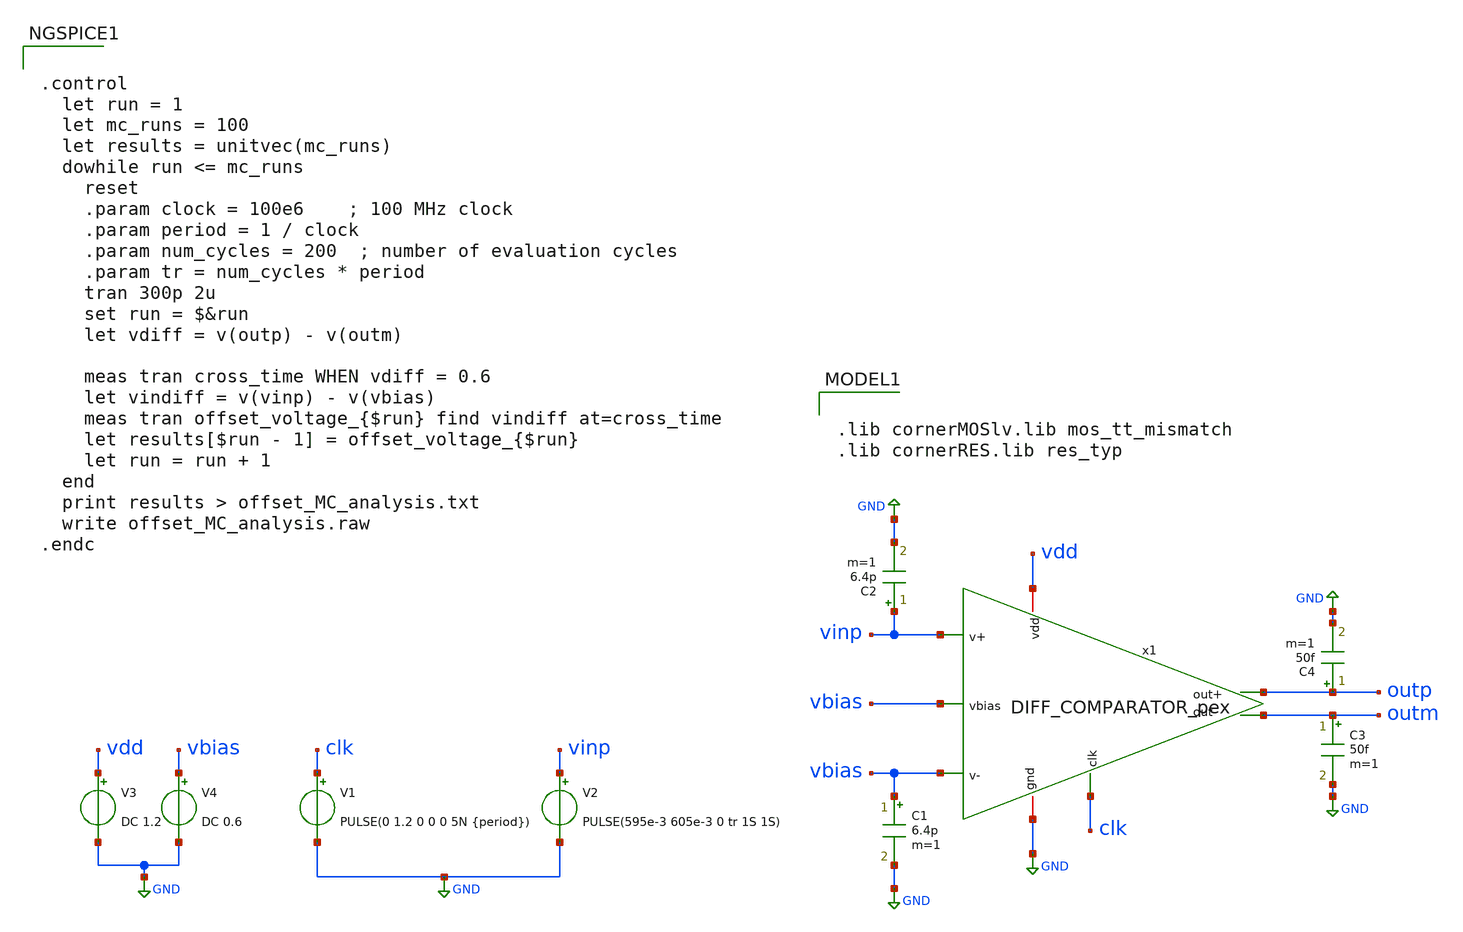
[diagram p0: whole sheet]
** sch_path: modules/module_3_8_bit_SAR_ADC/part_5_layout/comparator/xschem_post_layout/testbench/offset_MC_analysis.sch
**.subckt offset_MC_analysis
V3 vdd GND DC 1.2
V4 vbias GND DC 0.6
V1 clk GND PULSE(0 1.2 0 0 0 5N {period})
V2 vinp GND PULSE(595e-3 605e-3 0 tr 1S 1S)
C1 vbias GND 6.4p m=1
C2 vinp GND 6.4p m=1
C4 outp GND 50f m=1
C3 outm GND 50f m=1
x1 vdd vbias vinp vbias outm outp clk GND DIFF_COMPARATOR_pex
**** begin user architecture code

.lib cornerMOSlv.lib mos_tt_mismatch
.lib cornerRES.lib res_typ




.control
  let run = 1
  let mc_runs = 100
  let results = unitvec(mc_runs)
  dowhile run <= mc_runs
    reset
    .param clock = 100e6    ; 100 MHz clock
    .param period = 1 / clock
    .param num_cycles = 200  ; number of evaluation cycles
    .param tr = num_cycles * period
    tran 300p 2u
    set run = $&run
    let vdiff = v(outp) - v(outm)

    meas tran cross_time WHEN vdiff = 0.6
    let vindiff = v(vinp) - v(vbias)
    meas tran offset_voltage_{$run} find vindiff at=cross_time
    let results[$run - 1] = offset_voltage_{$run}
    let run = run + 1
  end
  print results > offset_MC_analysis.txt
  write offset_MC_analysis.raw
.endc



**** end user architecture code
**.ends

* expanding   symbol:
*+  /home/pedersen/projects/IHP-AnalogAcademy/modules/module_3_8_bit_SAR_ADC/part_5_layout/comparator/pex/xschem_pex_symbol/DIFF_COMPARATOR_pex.sym # of pins=8
** sym_path: modules/module_3_8_bit_SAR_ADC/part_5_layout/comparator/pex/xschem_pex_symbol/DIFF_COMPARATOR.sym

.subckt DIFF_COMPARATOR_pex vdd gnd V+ V- clk out- out+ vbias
X0 a_687_2445# V- a_1245_3300# vdd sg13_lv_pmos ad=0.76p pd=4.38u as=1.36p ps=8.68u w=4u l=0.2u M=8
X1 a_944_1911# V+ a_1245_3300# vdd sg13_lv_pmos ad=0.76p pd=4.38u as=1.36p ps=8.68u w=4u l=0.2u M=8
X2 a_1752_817# vbias vdd vdd sg13_lv_pmos ad=1.53p pd=9.68u as=0.855p ps=4.88u w=4.5u l=0.3u M=4
X3 gnd gnd gnd gnd sg13_lv_nmos ad=1.36p pd=8.68u as=50.9002p ps=0.15373m w=4u l=0.2u M=4
X4 vdd a_944_1911# out+ vdd sg13_lv_pmos ad=0.76p pd=4.38u as=1.36p ps=8.68u w=4u l=0.2u M=2
X5 a_944_1911# a_687_2445# gnd gnd sg13_lv_nmos ad=1.44p pd=4.72u as=0.76p ps=4.38u w=4u l=0.2u
X6 a_687_2445# clk gnd gnd sg13_lv_nmos ad=1.44p pd=4.72u as=0.76p ps=4.38u w=4u l=0.2u
X7 gnd a_944_1911# a_687_2445# gnd sg13_lv_nmos ad=0.76p pd=4.38u as=1.44p ps=4.72u w=4u l=0.2u
X8 out- a_687_2445# gnd gnd sg13_lv_nmos ad=0.68p pd=4.68u as=0.38p ps=2.38u w=2u l=0.2u M=2
X9 gnd clk a_944_1911# gnd sg13_lv_nmos ad=0.76p pd=4.38u as=1.44p ps=4.72u w=4u l=0.2u
X10 out- a_687_2445# vdd vdd sg13_lv_pmos ad=1.36p pd=8.68u as=0.76p ps=4.38u w=4u l=0.2u M=2
X11 out+ a_944_1911# gnd gnd sg13_lv_nmos ad=0.68p pd=4.68u as=0.38p ps=2.38u w=2u l=0.2u M=2
X12 a_1245_3300# clk a_1752_817# vdd sg13_lv_pmos ad=1.53p pd=9.68u as=0.855p ps=4.88u w=4.5u l=0.3u
+ M=4
C0 a_1752_817# a_1245_3300# 3.76533f
C1 a_944_1911# a_1245_3300# 8.04522f
C2 out- out+ 0.0933f
C3 clk a_1245_3300# 0.44782f
C4 w_805_2869# vdd 0.1537f
C5 V+ a_1245_3300# 0.76573f
C6 V- a_1245_3300# 0.94179f
C7 a_1245_3300# vdd 2.55093f
C8 a_944_1911# a_1752_817# 0.0558f
C9 a_1245_3300# a_687_2445# 11.3534f
C10 a_1752_817# vbias 2.28993f
C11 a_1752_817# clk 0.5025f
C12 a_944_1911# clk 0.24743f
C13 V+ a_944_1911# 1.08178f
C14 V- a_944_1911# 0.46901f
C15 a_1245_3300# out+ 0.36924f
C16 clk vbias 0.19878f
C17 a_1245_3300# out- 0.36795f
C18 a_1752_817# vdd 7.11146f
C19 a_1752_817# a_687_2445# 0.04531f
C20 a_944_1911# vdd 1.10862f
C21 a_944_1911# a_687_2445# 2.24936f
C22 vbias vdd 2.83964f
C23 clk vdd 2.98842f
C24 V- V+ 1.61045f
C25 clk a_687_2445# 0.23833f
C26 V+ vdd 4.08205f
C27 V- vdd 4.06121f
C28 V+ a_687_2445# 0.13025f
C29 V- a_687_2445# 0.78527f
C30 a_944_1911# out+ 0.80028f
C31 a_944_1911# out- 0.61161f
C32 a_687_2445# vdd 1.31156f
C33 vdd out+ 1.84773f
C34 a_687_2445# out+ 0.69286f
C35 vdd out- 1.84304f
C36 a_687_2445# out- 0.89453f
R0 V+.n6 V+.n0 17.1875
R1 V+.n6 V+.n5 16.5321
R2 V+.n2 V+.n1 15.8046
R3 V+.n4 V+.n3 9.60223
R4 V+.n4 V+.n1 8.28871
R5 V+.n3 V+.n0 8.28871
R6 V+.n5 V+.n4 7.51146
R7 V+.n3 V+.n2 7.51146
R8 V+ V+.n6 1.77098
R9 V-.n6 V-.n0 17.1792
R10 V-.n3 V-.n0 17.1129
R11 V-.n4 V-.n1 17.1083
R12 V-.n6 V-.n5 16.5321
R13 V-.n2 V-.n1 15.8156
R14 V-.n5 V-.n4 7.51146
R15 V-.n3 V-.n2 7.51146
R16 V- V-.n6 1.57783
R17 V-.n4 V-.n3 0.792909
R18 vbias vbias.n0 6.1153
R19 out-.n17 out-.n1 17.0005
R20 out-.n22 out-.n1 17.0005
R21 out-.n13 out-.n1 17.0005
R22 out-.n35 out-.n7 17.0005
R23 out-.n35 out-.n6 17.0005
R24 out-.n35 out-.n8 17.0005
R25 out-.n42 out-.n41 9.04081
R26 out-.n12 out-.n10 9.03703
R27 out-.n24 out-.n23 9.0005
R28 out-.n21 out-.n20 9.0005
R29 out-.n16 out-.n3 9.0005
R30 out-.n40 out-.n39 9.0005
R31 out-.n31 out-.n30 9.0005
R32 out-.n28 out-.n27 9.0005
R33 out-.n45 out-.n43 9.0005
R34 out-.n46 out-.n43 9.0005
R35 out-.n44 out-.n43 9.0005
R36 out-.n51 out-.n43 9.0005
R37 out-.n52 out-.n45 9.0005
R38 out-.n52 out-.n46 9.0005
R39 out-.n52 out-.n44 9.0005
R40 out-.n52 out-.n51 9.0005
R41 out-.n36 out-.n35 8.501
R42 out-.n12 out-.n1 8.50006
R43 out-.n35 out-.n5 8.49923
R44 out-.n50 out-.n49 8.49864
R45 out-.n49 out-.n47 8.49864
R46 out-.n41 out-.n1 8.49628
R47 out-.n49 out-.n48 8.49096
R48 out-.n35 out-.n4 8.49007
R49 out-.n35 out-.n34 8.49007
R50 out-.n2 out-.n1 8.46606
R51 out-.n29 out-.n1 8.46606
R52 out-.n10 out-.n5 4.51473
R53 out-.n36 out-.n0 4.51194
R54 out-.n38 out-.n37 4.5005
R55 out-.n19 out-.n18 4.5005
R56 out-.n15 out-.n14 4.5005
R57 out-.n26 out-.n25 4.5005
R58 out-.n11 out-.n9 4.5005
R59 out-.n33 out-.n32 4.5005
R60 out- out-.n53 1.4685
R61 out-.n30 out-.n12 0.146886
R62 out-.n41 out-.n40 0.143078
R63 out-.n17 out-.n16 0.137052
R64 out-.n28 out-.n13 0.129466
R65 out-.n53 out-.n42 0.126844
R66 out-.n40 out-.n2 0.108815
R67 out-.n30 out-.n29 0.101229
R68 out-.n22 out-.n21 0.0953276
R69 out-.n23 out-.n22 0.0877414
R70 out-.n29 out-.n28 0.0822633
R71 out-.n16 out-.n2 0.0746771
R72 out-.n23 out-.n13 0.0536034
R73 out-.n37 out-.n36 0.0468193
R74 out-.n21 out-.n17 0.0460172
R75 out-.n50 out-.n44 0.0453402
R76 out-.n47 out-.n46 0.0453402
R77 out-.n33 out-.n5 0.0450428
R78 out-.n9 out-.n8 0.043672
R79 out-.n18 out-.n7 0.0401237
R80 out-.n34 out-.n33 0.0352729
R81 out-.n37 out-.n4 0.0317246
R82 out-.n25 out-.n6 0.0306613
R83 out-.n48 out-.n44 0.0293633
R84 out-.n48 out-.n46 0.0293633
R85 out-.n14 out-.n6 0.0271129
R86 out-.n18 out-.n4 0.0269934
R87 out-.n34 out-.n9 0.023445
R88 out-.n32 out-.n10 0.019037
R89 out-.n31 out-.n11 0.019037
R90 out-.n27 out-.n26 0.019037
R91 out-.n24 out-.n15 0.019037
R92 out-.n20 out-.n19 0.019037
R93 out-.n38 out-.n3 0.019037
R94 out-.n39 out-.n0 0.019037
R95 out-.n14 out-.n7 0.0176505
R96 out-.n25 out-.n8 0.0141022
R97 out-.n51 out-.n50 0.0134159
R98 out-.n47 out-.n45 0.0134159
R99 out-.n53 out-.n43 0.0127081
R100 out-.n53 out-.n52 0.0127081
R101 out-.n32 out-.n31 0.00151852
R102 out-.n27 out-.n11 0.00151852
R103 out-.n26 out-.n24 0.00151852
R104 out-.n20 out-.n15 0.00151852
R105 out-.n19 out-.n3 0.00151852
R106 out-.n39 out-.n38 0.00151852
R107 out-.n42 out-.n0 0.00151852
R108 out+.n40 out+.n5 17.0005
R109 out+.n40 out+.n2 17.0005
R110 out+.n40 out+.n6 17.0005
R111 out+.n34 out+.n33 17.0005
R112 out+.n33 out+.n14 17.0005
R113 out+.n33 out+.n17 17.0005
R114 out+.n29 out+.n4 9.04081
R115 out+.n42 out+.n41 9.03703
R116 out+.n10 out+.n9 9.0005
R117 out+.n21 out+.n20 9.0005
R118 out+.n25 out+.n24 9.0005
R119 out+.n28 out+.n27 9.0005
R120 out+.n7 out+.n1 9.0005
R121 out+.n38 out+.n37 9.0005
R122 out+.n45 out+.n43 9.0005
R123 out+.n46 out+.n43 9.0005
R124 out+.n44 out+.n43 9.0005
R125 out+.n51 out+.n43 9.0005
R126 out+.n52 out+.n45 9.0005
R127 out+.n52 out+.n46 9.0005
R128 out+.n52 out+.n44 9.0005
R129 out+.n52 out+.n51 9.0005
R130 out+.n33 out+.n16 8.501
R131 out+.n41 out+.n40 8.50006
R132 out+.n33 out+.n13 8.49923
R133 out+.n49 out+.n47 8.49864
R134 out+.n50 out+.n49 8.49864
R135 out+.n40 out+.n4 8.49628
R136 out+.n49 out+.n48 8.49096
R137 out+.n33 out+.n11 8.49007
R138 out+.n33 out+.n32 8.49007
R139 out+.n40 out+.n3 8.46606
R140 out+.n40 out+.n39 8.46606
R141 out+.n29 out+.n13 4.51392
R142 out+.n16 out+.n0 4.51194
R143 out+.n31 out+.n30 4.5005
R144 out+.n26 out+.n18 4.5005
R145 out+.n23 out+.n22 4.5005
R146 out+.n19 out+.n12 4.5005
R147 out+.n36 out+.n35 4.5005
R148 out+.n15 out+.n8 4.5005
R149 out+ out+.n53 1.36221
R150 out+.n41 out+.n1 0.146886
R151 out+.n27 out+.n4 0.143078
R152 out+.n24 out+.n5 0.137052
R153 out+.n38 out+.n6 0.129466
R154 out+.n53 out+.n42 0.127659
R155 out+.n27 out+.n3 0.108815
R156 out+.n39 out+.n1 0.101229
R157 out+.n20 out+.n2 0.0953276
R158 out+.n9 out+.n2 0.0877414
R159 out+.n39 out+.n38 0.0822633
R160 out+.n24 out+.n3 0.0746771
R161 out+.n9 out+.n6 0.0536034
R162 out+.n16 out+.n15 0.0468193
R163 out+.n20 out+.n5 0.0460172
R164 out+.n50 out+.n44 0.0453402
R165 out+.n47 out+.n46 0.0453402
R166 out+.n31 out+.n13 0.0450428
R167 out+.n18 out+.n17 0.043672
R168 out+.n35 out+.n34 0.0401237
R169 out+.n32 out+.n31 0.0352729
R170 out+.n15 out+.n11 0.0317246
R171 out+.n22 out+.n14 0.0306613
R172 out+.n48 out+.n44 0.0293633
R173 out+.n48 out+.n46 0.0293633
R174 out+.n14 out+.n12 0.0271129
R175 out+.n35 out+.n11 0.0269934
R176 out+.n32 out+.n18 0.023445
R177 out+.n7 out+.n0 0.0198519
R178 out+.n37 out+.n8 0.0198519
R179 out+.n36 out+.n10 0.0198519
R180 out+.n21 out+.n19 0.0198519
R181 out+.n25 out+.n23 0.0198519
R182 out+.n28 out+.n26 0.0198519
R183 out+.n30 out+.n29 0.0198519
R184 out+.n34 out+.n12 0.0176505
R185 out+.n22 out+.n17 0.0141022
R186 out+.n51 out+.n50 0.0134159
R187 out+.n47 out+.n45 0.0134159
R188 out+.n53 out+.n43 0.0127081
R189 out+.n53 out+.n52 0.0127081
R190 out+.n42 out+.n0 0.000703704
R191 out+.n8 out+.n7 0.000703704
R192 out+.n37 out+.n36 0.000703704
R193 out+.n19 out+.n10 0.000703704
R194 out+.n23 out+.n21 0.000703704
R195 out+.n26 out+.n25 0.000703704
R196 out+.n30 out+.n28 0.000703704
R197 clk.n4 clk.n0 32.251
R198 clk.n3 clk.n2 29.4509
R199 clk.n3 clk.n1 12.2999
R200 clk.n4 clk.n3 2.20443
R201 clk clk.n4 0.574117
R202 vdd.n208 vdd.n190 17.0005
R203 vdd.n208 vdd.n188 17.0005
R204 vdd.n208 vdd.n191 17.0005
R205 vdd.n208 vdd.n186 17.0005
R206 vdd.n208 vdd.n207 17.0005
R207 vdd.n239 vdd.n178 17.0005
R208 vdd.n179 vdd.n178 17.0005
R209 vdd.n232 vdd.n178 17.0005
R210 vdd.n227 vdd.n178 17.0005
R211 vdd.n225 vdd.n178 17.0005
R212 vdd.n210 vdd.n209 9.05964
R213 vdd.n189 vdd.n176 9.05964
R214 vdd.n222 vdd.n183 9.05964
R215 vdd.n242 vdd.n241 9.05964
R216 vdd.n226 vdd.n182 9.0005
R217 vdd.n229 vdd.n228 9.0005
R218 vdd.n231 vdd.n230 9.0005
R219 vdd.n233 vdd.n180 9.0005
R220 vdd.n236 vdd.n235 9.0005
R221 vdd.n238 vdd.n237 9.0005
R222 vdd.n240 vdd.n177 9.0005
R223 vdd.n224 vdd.n223 9.0005
R224 vdd.n206 vdd.n205 9.0005
R225 vdd.n204 vdd.n203 9.0005
R226 vdd.n202 vdd.n201 9.0005
R227 vdd.n200 vdd.n199 9.0005
R228 vdd.n198 vdd.n197 9.0005
R229 vdd.n196 vdd.n195 9.0005
R230 vdd.n194 vdd.n193 9.0005
R231 vdd.n185 vdd.n184 9.0005
R232 vdd.n128 vdd.n127 8.501
R233 vdd.n115 vdd.n89 8.501
R234 vdd.n98 vdd.n97 8.501
R235 vdd.n81 vdd.n80 8.501
R236 vdd.n134 vdd.n69 8.501
R237 vdd.n208 vdd.n189 8.47918
R238 vdd.n208 vdd.n187 8.47918
R239 vdd.n208 vdd.n192 8.47918
R240 vdd.n209 vdd.n208 8.47918
R241 vdd.n241 vdd.n178 8.47918
R242 vdd.n234 vdd.n178 8.47918
R243 vdd.n181 vdd.n178 8.47918
R244 vdd.n183 vdd.n178 8.47918
R245 vdd.n87 vdd.n86 5.66778
R246 vdd.n243 vdd.n176 5.20536
R247 vdd.n221 vdd.n210 5.20536
R248 vdd.n222 vdd.n221 4.6895
R249 vdd.n243 vdd.n242 4.6895
R250 vdd.n245 vdd.n173 4.56174
R251 vdd.n249 vdd.n174 4.56174
R252 vdd.n215 vdd.n211 4.56174
R253 vdd.n219 vdd.n212 4.56174
R254 vdd.n165 vdd.n2 4.56174
R255 vdd.n169 vdd.n3 4.56174
R256 vdd.n11 vdd.n7 4.56174
R257 vdd.n15 vdd.n8 4.56174
R258 vdd.n28 vdd.n25 4.56174
R259 vdd.n32 vdd.n26 4.56174
R260 vdd.n38 vdd.n35 4.56174
R261 vdd.n42 vdd.n36 4.56174
R262 vdd.n48 vdd.n45 4.56174
R263 vdd.n52 vdd.n46 4.56174
R264 vdd.n136 vdd.n66 4.56174
R265 vdd.n140 vdd.n67 4.56174
R266 vdd.n74 vdd.n70 4.56174
R267 vdd.n78 vdd.n71 4.56174
R268 vdd.n100 vdd.n93 4.56174
R269 vdd.n104 vdd.n94 4.56174
R270 vdd.n109 vdd.n90 4.56174
R271 vdd.n113 vdd.n91 4.56174
R272 vdd.n121 vdd.n117 4.56174
R273 vdd.n125 vdd.n118 4.56174
R274 vdd.n145 vdd.n22 4.56174
R275 vdd.n149 vdd.n23 4.56174
R276 vdd.n58 vdd.n55 4.56174
R277 vdd.n62 vdd.n56 4.56174
R278 vdd.n248 vdd.n247 4.5005
R279 vdd.n246 vdd.n175 4.5005
R280 vdd.n218 vdd.n217 4.5005
R281 vdd.n216 vdd.n213 4.5005
R282 vdd.n166 vdd.n4 4.5005
R283 vdd.n168 vdd.n167 4.5005
R284 vdd.n12 vdd.n9 4.5005
R285 vdd.n14 vdd.n13 4.5005
R286 vdd.n29 vdd.n27 4.5005
R287 vdd.n31 vdd.n30 4.5005
R288 vdd.n39 vdd.n37 4.5005
R289 vdd.n41 vdd.n40 4.5005
R290 vdd.n49 vdd.n47 4.5005
R291 vdd.n51 vdd.n50 4.5005
R292 vdd.n137 vdd.n68 4.5005
R293 vdd.n139 vdd.n138 4.5005
R294 vdd.n75 vdd.n72 4.5005
R295 vdd.n77 vdd.n76 4.5005
R296 vdd.n101 vdd.n95 4.5005
R297 vdd.n103 vdd.n102 4.5005
R298 vdd.n110 vdd.n92 4.5005
R299 vdd.n112 vdd.n111 4.5005
R300 vdd.n122 vdd.n119 4.5005
R301 vdd.n124 vdd.n123 4.5005
R302 vdd.n146 vdd.n24 4.5005
R303 vdd.n148 vdd.n147 4.5005
R304 vdd.n59 vdd.n57 4.5005
R305 vdd.n61 vdd.n60 4.5005
R306 vdd.n133 vdd.n132 4.16092
R307 vdd.n116 vdd.n82 4.16066
R308 vdd.n96 vdd.n84 4.16066
R309 vdd.n88 vdd.n83 4.16054
R310 vdd.n154 vdd.n6 4.16048
R311 vdd.n158 vdd.n6 4.16048
R312 vdd.n162 vdd.n6 4.16048
R313 vdd.n131 vdd.n82 2.83383
R314 vdd.n131 vdd.n83 2.83383
R315 vdd.n131 vdd.n84 2.83383
R316 vdd.n132 vdd.n131 2.83383
R317 vdd.n21 vdd.n6 2.7354
R318 vdd.n245 vdd.n244 2.28117
R319 vdd.n244 vdd.n174 2.28117
R320 vdd.n220 vdd.n211 2.28117
R321 vdd.n220 vdd.n219 2.28117
R322 vdd.n165 vdd.n164 2.28117
R323 vdd.n164 vdd.n3 2.28117
R324 vdd.n16 vdd.n7 2.28117
R325 vdd.n16 vdd.n15 2.28117
R326 vdd.n28 vdd.n17 2.28117
R327 vdd.n26 vdd.n17 2.28117
R328 vdd.n38 vdd.n18 2.28117
R329 vdd.n36 vdd.n18 2.28117
R330 vdd.n48 vdd.n19 2.28117
R331 vdd.n46 vdd.n19 2.28117
R332 vdd.n136 vdd.n135 2.28117
R333 vdd.n135 vdd.n67 2.28117
R334 vdd.n79 vdd.n70 2.28117
R335 vdd.n79 vdd.n78 2.28117
R336 vdd.n100 vdd.n99 2.28117
R337 vdd.n99 vdd.n94 2.28117
R338 vdd.n114 vdd.n90 2.28117
R339 vdd.n114 vdd.n113 2.28117
R340 vdd.n126 vdd.n117 2.28117
R341 vdd.n126 vdd.n125 2.28117
R342 vdd.n150 vdd.n22 2.28117
R343 vdd.n150 vdd.n149 2.28117
R344 vdd.n58 vdd.n20 2.28117
R345 vdd.n56 vdd.n20 2.28117
R346 vdd.n250 vdd.n173 2.25769
R347 vdd.n250 vdd.n249 2.25769
R348 vdd.n215 vdd.n214 2.25769
R349 vdd.n214 vdd.n212 2.25769
R350 vdd.n170 vdd.n2 2.25769
R351 vdd.n170 vdd.n169 2.25769
R352 vdd.n11 vdd.n10 2.25769
R353 vdd.n10 vdd.n8 2.25769
R354 vdd.n33 vdd.n25 2.25769
R355 vdd.n33 vdd.n32 2.25769
R356 vdd.n43 vdd.n35 2.25769
R357 vdd.n43 vdd.n42 2.25769
R358 vdd.n53 vdd.n45 2.25769
R359 vdd.n53 vdd.n52 2.25769
R360 vdd.n141 vdd.n66 2.25769
R361 vdd.n141 vdd.n140 2.25769
R362 vdd.n74 vdd.n73 2.25769
R363 vdd.n73 vdd.n71 2.25769
R364 vdd.n105 vdd.n93 2.25769
R365 vdd.n105 vdd.n104 2.25769
R366 vdd.n109 vdd.n108 2.25769
R367 vdd.n108 vdd.n91 2.25769
R368 vdd.n121 vdd.n120 2.25769
R369 vdd.n120 vdd.n118 2.25769
R370 vdd.n145 vdd.n144 2.25769
R371 vdd.n144 vdd.n23 2.25769
R372 vdd.n63 vdd.n55 2.25769
R373 vdd.n63 vdd.n62 2.25769
R374 vdd.n156 vdd.n6 1.99818
R375 vdd.n160 vdd.n6 1.9981
R376 vdd.n244 vdd.n243 1.89937
R377 vdd.n221 vdd.n220 1.89937
R378 vdd.n164 vdd.n163 1.66843
R379 vdd.n161 vdd.n16 1.66843
R380 vdd.n159 vdd.n17 1.66843
R381 vdd.n157 vdd.n18 1.66843
R382 vdd.n155 vdd.n19 1.66843
R383 vdd.n135 vdd.n134 1.66843
R384 vdd.n80 vdd.n79 1.66843
R385 vdd.n99 vdd.n98 1.66843
R386 vdd.n115 vdd.n114 1.66843
R387 vdd.n127 vdd.n126 1.66843
R388 vdd.n151 vdd.n150 1.66843
R389 vdd.n153 vdd.n20 1.66843
R390 vdd.n152 vdd.n151 1.52562
R391 vdd.n153 vdd.n152 1.2834
R392 vdd.n86 vdd.n5 1.27296
R393 vdd.n86 vdd.n85 1.21158
R394 vdd.n64 vdd.n63 1.1005
R395 vdd.n54 vdd.n53 1.1005
R396 vdd.n44 vdd.n43 1.1005
R397 vdd.n34 vdd.n33 1.1005
R398 vdd.n10 vdd.n1 1.1005
R399 vdd.n171 vdd.n170 1.1005
R400 vdd.n144 vdd.n143 1.1005
R401 vdd.n120 vdd.n0 1.1005
R402 vdd.n108 vdd.n107 1.1005
R403 vdd.n106 vdd.n105 1.1005
R404 vdd.n73 vdd.n65 1.1005
R405 vdd.n142 vdd.n141 1.1005
R406 vdd.n214 vdd.n172 1.1005
R407 vdd.n251 vdd.n250 1.1005
R408 vdd.n127 vdd.n85 1.0667
R409 vdd.n163 vdd.n5 0.897218
R410 vdd.n130 vdd.n129 0.740086
R411 vdd.n129 vdd.n85 0.513736
R412 vdd.n6 vdd.n5 0.434488
R413 vdd.n134 vdd.n21 0.405564
R414 vdd.n127 vdd.n116 0.338749
R415 vdd.n163 vdd.n162 0.338361
R416 vdd.n115 vdd.n88 0.332914
R417 vdd.n98 vdd.n96 0.328172
R418 vdd.n159 vdd.n158 0.327784
R419 vdd.n133 vdd.n80 0.322902
R420 vdd.n155 vdd.n154 0.317207
R421 vdd.n161 vdd.n160 0.30387
R422 vdd.n157 vdd.n156 0.29911
R423 vdd.n156 vdd.n155 0.273116
R424 vdd.n154 vdd.n153 0.272784
R425 vdd.n160 vdd.n159 0.268235
R426 vdd.n134 vdd.n133 0.267129
R427 vdd.n158 vdd.n157 0.262207
R428 vdd.n96 vdd.n80 0.261823
R429 vdd.n98 vdd.n88 0.257063
R430 vdd.n162 vdd.n161 0.25163
R431 vdd.n116 vdd.n115 0.251246
R432 vdd.n143 vdd.n64 0.245476
R433 vdd.n172 vdd.n171 0.223305
R434 vdd.n130 vdd.n6 0.187367
R435 vdd.n151 vdd.n21 0.179715
R436 vdd.n252 vdd.n0 0.142854
R437 vdd.n223 vdd.n222 0.0965
R438 vdd.n223 vdd.n182 0.0965
R439 vdd.n229 vdd.n182 0.0965
R440 vdd.n230 vdd.n229 0.0965
R441 vdd.n230 vdd.n180 0.0965
R442 vdd.n236 vdd.n180 0.0965
R443 vdd.n237 vdd.n236 0.0965
R444 vdd.n237 vdd.n177 0.0965
R445 vdd.n242 vdd.n177 0.0965
R446 vdd.n210 vdd.n184 0.0965
R447 vdd.n205 vdd.n184 0.0965
R448 vdd.n205 vdd.n204 0.0965
R449 vdd.n204 vdd.n202 0.0965
R450 vdd.n202 vdd.n200 0.0965
R451 vdd.n200 vdd.n198 0.0965
R452 vdd.n198 vdd.n196 0.0965
R453 vdd.n196 vdd.n194 0.0965
R454 vdd.n194 vdd.n176 0.0965
R455 vdd.n152 vdd.n6 0.0898978
R456 vdd.n203 vdd.n186 0.083
R457 vdd.n197 vdd.n188 0.083
R458 vdd.n228 vdd.n227 0.083
R459 vdd.n235 vdd.n179 0.083
R460 vdd.n252 vdd.n251 0.0809512
R461 vdd.n201 vdd.n192 0.0721377
R462 vdd.n199 vdd.n187 0.0721377
R463 vdd.n231 vdd.n181 0.0721377
R464 vdd.n234 vdd.n233 0.0721377
R465 vdd.n207 vdd.n185 0.0705
R466 vdd.n193 vdd.n190 0.0705
R467 vdd.n225 vdd.n224 0.0705
R468 vdd.n240 vdd.n239 0.0705
R469 vdd.n209 vdd.n185 0.0621377
R470 vdd.n193 vdd.n189 0.0621377
R471 vdd.n224 vdd.n183 0.0621377
R472 vdd.n241 vdd.n240 0.0621377
R473 vdd.n248 vdd.n175 0.0608429
R474 vdd.n247 vdd.n246 0.0608429
R475 vdd.n218 vdd.n213 0.0608429
R476 vdd.n217 vdd.n216 0.0608429
R477 vdd.n168 vdd.n4 0.0608429
R478 vdd.n167 vdd.n166 0.0608429
R479 vdd.n13 vdd.n12 0.0608429
R480 vdd.n14 vdd.n9 0.0608429
R481 vdd.n31 vdd.n27 0.0608429
R482 vdd.n30 vdd.n29 0.0608429
R483 vdd.n41 vdd.n37 0.0608429
R484 vdd.n40 vdd.n39 0.0608429
R485 vdd.n51 vdd.n47 0.0608429
R486 vdd.n50 vdd.n49 0.0608429
R487 vdd.n139 vdd.n68 0.0608429
R488 vdd.n138 vdd.n137 0.0608429
R489 vdd.n76 vdd.n75 0.0608429
R490 vdd.n77 vdd.n72 0.0608429
R491 vdd.n103 vdd.n95 0.0608429
R492 vdd.n102 vdd.n101 0.0608429
R493 vdd.n111 vdd.n110 0.0608429
R494 vdd.n112 vdd.n92 0.0608429
R495 vdd.n123 vdd.n122 0.0608429
R496 vdd.n124 vdd.n119 0.0608429
R497 vdd.n147 vdd.n146 0.0608429
R498 vdd.n148 vdd.n24 0.0608429
R499 vdd.n60 vdd.n59 0.0608429
R500 vdd.n61 vdd.n57 0.0608429
R501 vdd.n201 vdd.n191 0.0605
R502 vdd.n199 vdd.n191 0.0605
R503 vdd.n232 vdd.n231 0.0605
R504 vdd.n233 vdd.n232 0.0605
R505 vdd.n251 vdd.n172 0.0577927
R506 vdd.n207 vdd.n206 0.0505
R507 vdd.n195 vdd.n190 0.0505
R508 vdd.n226 vdd.n225 0.0505
R509 vdd.n239 vdd.n238 0.0505
R510 vdd.n203 vdd.n192 0.0496377
R511 vdd.n197 vdd.n187 0.0496377
R512 vdd.n228 vdd.n181 0.0496377
R513 vdd.n235 vdd.n234 0.0496377
R514 vdd.n206 vdd.n186 0.038
R515 vdd.n195 vdd.n188 0.038
R516 vdd.n227 vdd.n226 0.038
R517 vdd.n238 vdd.n179 0.038
R518 vdd.n249 vdd.n248 0.0308751
R519 vdd.n175 vdd.n173 0.0308751
R520 vdd.n217 vdd.n212 0.0308751
R521 vdd.n216 vdd.n215 0.0308751
R522 vdd.n4 vdd.n2 0.0308751
R523 vdd.n169 vdd.n168 0.0308751
R524 vdd.n12 vdd.n11 0.0308751
R525 vdd.n13 vdd.n8 0.0308751
R526 vdd.n27 vdd.n25 0.0308751
R527 vdd.n32 vdd.n31 0.0308751
R528 vdd.n37 vdd.n35 0.0308751
R529 vdd.n42 vdd.n41 0.0308751
R530 vdd.n47 vdd.n45 0.0308751
R531 vdd.n52 vdd.n51 0.0308751
R532 vdd.n68 vdd.n66 0.0308751
R533 vdd.n140 vdd.n139 0.0308751
R534 vdd.n75 vdd.n74 0.0308751
R535 vdd.n76 vdd.n71 0.0308751
R536 vdd.n95 vdd.n93 0.0308751
R537 vdd.n104 vdd.n103 0.0308751
R538 vdd.n110 vdd.n109 0.0308751
R539 vdd.n111 vdd.n91 0.0308751
R540 vdd.n122 vdd.n121 0.0308751
R541 vdd.n123 vdd.n118 0.0308751
R542 vdd.n146 vdd.n145 0.0308751
R543 vdd.n147 vdd.n23 0.0308751
R544 vdd.n57 vdd.n55 0.0308751
R545 vdd.n62 vdd.n61 0.0308751
R546 vdd.n247 vdd.n174 0.0307722
R547 vdd.n246 vdd.n245 0.0307722
R548 vdd.n219 vdd.n218 0.0307722
R549 vdd.n213 vdd.n211 0.0307722
R550 vdd.n166 vdd.n165 0.0307722
R551 vdd.n167 vdd.n3 0.0307722
R552 vdd.n9 vdd.n7 0.0307722
R553 vdd.n15 vdd.n14 0.0307722
R554 vdd.n29 vdd.n28 0.0307722
R555 vdd.n30 vdd.n26 0.0307722
R556 vdd.n39 vdd.n38 0.0307722
R557 vdd.n40 vdd.n36 0.0307722
R558 vdd.n49 vdd.n48 0.0307722
R559 vdd.n50 vdd.n46 0.0307722
R560 vdd.n137 vdd.n136 0.0307722
R561 vdd.n138 vdd.n67 0.0307722
R562 vdd.n72 vdd.n70 0.0307722
R563 vdd.n78 vdd.n77 0.0307722
R564 vdd.n101 vdd.n100 0.0307722
R565 vdd.n102 vdd.n94 0.0307722
R566 vdd.n92 vdd.n90 0.0307722
R567 vdd.n113 vdd.n112 0.0307722
R568 vdd.n119 vdd.n117 0.0307722
R569 vdd.n125 vdd.n124 0.0307722
R570 vdd.n24 vdd.n22 0.0307722
R571 vdd.n149 vdd.n148 0.0307722
R572 vdd.n59 vdd.n58 0.0307722
R573 vdd.n60 vdd.n56 0.0307722
R574 vdd.n64 vdd.n54 0.0235488
R575 vdd.n54 vdd.n44 0.0235488
R576 vdd.n44 vdd.n34 0.0235488
R577 vdd.n34 vdd.n1 0.0235488
R578 vdd.n171 vdd.n1 0.0235488
R579 vdd.n143 vdd.n142 0.0235488
R580 vdd.n142 vdd.n65 0.0235488
R581 vdd.n106 vdd.n65 0.0235488
R582 vdd.n107 vdd.n106 0.0235488
R583 vdd.n107 vdd.n0 0.0235488
R584 vdd.n131 vdd.n130 0.00773882
R585 vdd vdd.n252 0.00527439
R586 vdd.n87 vdd.n6 0.00166667
R587 vdd.n129 vdd.n87 0.00133332
R588 vdd.n69 vdd.n6 0.001
R589 vdd.n132 vdd.n81 0.001
R590 vdd.n97 vdd.n84 0.001
R591 vdd.n89 vdd.n83 0.001
R592 vdd.n128 vdd.n82 0.001
R593 vdd.n129 vdd.n128 0.001
R594 vdd.n89 vdd.n82 0.001
R595 vdd.n97 vdd.n83 0.001
R596 vdd.n84 vdd.n81 0.001
R597 vdd.n132 vdd.n69 0.001
R598 gnd.n82 gnd.n81 2794.14
R599 gnd.n12 gnd.n11 17.0005
R600 gnd.n74 gnd.n64 17.0005
R601 gnd.n65 gnd.n64 17.0005
R602 gnd.n73 gnd.n64 17.0005
R603 gnd.n66 gnd.n64 17.0005
R604 gnd.n72 gnd.n64 17.0005
R605 gnd.n67 gnd.n64 17.0005
R606 gnd.n71 gnd.n64 17.0005
R607 gnd.n68 gnd.n64 17.0005
R608 gnd.n70 gnd.n64 17.0005
R609 gnd.n69 gnd.n64 17.0005
R610 gnd.n76 gnd.n64 17.0005
R611 gnd.n75 gnd.n74 17.0005
R612 gnd.n75 gnd.n65 17.0005
R613 gnd.n75 gnd.n73 17.0005
R614 gnd.n75 gnd.n66 17.0005
R615 gnd.n75 gnd.n72 17.0005
R616 gnd.n75 gnd.n67 17.0005
R617 gnd.n75 gnd.n71 17.0005
R618 gnd.n75 gnd.n68 17.0005
R619 gnd.n75 gnd.n70 17.0005
R620 gnd.n75 gnd.n69 17.0005
R621 gnd.n76 gnd.n75 17.0005
R622 gnd.n35 gnd.n34 17.0005
R623 gnd.n34 gnd.n33 17.0005
R624 gnd.n81 gnd.n53 17.0005
R625 gnd.n81 gnd.n54 17.0005
R626 gnd.n81 gnd.n55 17.0005
R627 gnd.n81 gnd.n56 17.0005
R628 gnd.n81 gnd.n57 17.0005
R629 gnd.n81 gnd.n58 17.0005
R630 gnd.n81 gnd.n59 17.0005
R631 gnd.n81 gnd.n60 17.0005
R632 gnd.n81 gnd.n61 17.0005
R633 gnd.n81 gnd.n62 17.0005
R634 gnd.n124 gnd.n108 17.0005
R635 gnd.n109 gnd.n108 17.0005
R636 gnd.n122 gnd.n108 17.0005
R637 gnd.n110 gnd.n108 17.0005
R638 gnd.n121 gnd.n108 17.0005
R639 gnd.n111 gnd.n108 17.0005
R640 gnd.n120 gnd.n108 17.0005
R641 gnd.n112 gnd.n108 17.0005
R642 gnd.n119 gnd.n108 17.0005
R643 gnd.n113 gnd.n108 17.0005
R644 gnd.n118 gnd.n108 17.0005
R645 gnd.n124 gnd.n123 17.0005
R646 gnd.n123 gnd.n109 17.0005
R647 gnd.n123 gnd.n122 17.0005
R648 gnd.n123 gnd.n110 17.0005
R649 gnd.n123 gnd.n121 17.0005
R650 gnd.n123 gnd.n111 17.0005
R651 gnd.n123 gnd.n120 17.0005
R652 gnd.n123 gnd.n112 17.0005
R653 gnd.n123 gnd.n119 17.0005
R654 gnd.n123 gnd.n113 17.0005
R655 gnd.n123 gnd.n118 17.0005
R656 gnd.n126 gnd.n85 17.0005
R657 gnd.n126 gnd.n86 17.0005
R658 gnd.n126 gnd.n87 17.0005
R659 gnd.n126 gnd.n88 17.0005
R660 gnd.n126 gnd.n89 17.0005
R661 gnd.n126 gnd.n90 17.0005
R662 gnd.n126 gnd.n91 17.0005
R663 gnd.n126 gnd.n92 17.0005
R664 gnd.n126 gnd.n93 17.0005
R665 gnd.n126 gnd.n94 17.0005
R666 gnd.n10 gnd.n9 15.0005
R667 gnd.n78 gnd.n77 15.0005
R668 gnd.n32 gnd.n31 15.0005
R669 gnd.n116 gnd.n115 15.0005
R670 gnd.n101 gnd.n19 8.501
R671 gnd.n101 gnd.n95 8.501
R672 gnd.n101 gnd.n100 8.501
R673 gnd.n101 gnd.n99 8.501
R674 gnd.n102 gnd.n101 8.501
R675 gnd.n28 gnd.n24 8.49127
R676 gnd.n28 gnd.n27 8.49127
R677 gnd.n29 gnd.n28 8.49127
R678 gnd.n34 gnd.n25 8.49127
R679 gnd.n34 gnd.n26 8.49127
R680 gnd.n15 gnd.n14 8.49123
R681 gnd.n14 gnd.n7 8.49123
R682 gnd.n14 gnd.n13 8.49123
R683 gnd.n11 gnd.n6 8.49123
R684 gnd.n11 gnd.n8 8.49123
R685 gnd.n104 gnd.n103 8.48464
R686 gnd.n107 gnd.n96 8.46519
R687 gnd.n106 gnd.n97 8.46519
R688 gnd.n105 gnd.n98 8.46519
R689 gnd.n126 gnd.n18 8.34456
R690 gnd.n101 gnd.n82 6.02053
R691 gnd.n45 gnd.n44 5.48318
R692 gnd.n129 gnd.n128 5.48318
R693 gnd.n41 gnd.n40 5.47768
R694 gnd.n51 gnd.n50 5.47768
R695 gnd.n14 gnd.n5 3.4169
R696 gnd.n28 gnd.n23 3.4022
R697 gnd.n34 gnd.n23 3.40192
R698 gnd.n126 gnd.n125 3.3033
R699 gnd.n126 gnd.n84 3.29867
R700 gnd.n127 gnd.n126 3.29859
R701 gnd.n81 gnd.n80 3.29855
R702 gnd.n81 gnd.n21 3.29832
R703 gnd.n126 gnd.n3 3.28305
R704 gnd.n81 gnd.n22 3.28288
R705 gnd.n11 gnd.n5 2.82281
R706 gnd.n126 gnd.n83 2.69969
R707 gnd.n81 gnd.n20 2.6991
R708 gnd.n126 gnd.n17 1.94103
R709 gnd.n81 gnd.n37 1.94046
R710 gnd.n126 gnd.n82 1.53748
R711 gnd.n52 gnd.n51 1.20601
R712 gnd.n50 gnd.n43 1.10932
R713 gnd.n45 gnd.n0 1.10932
R714 gnd.n42 gnd.n41 1.10932
R715 gnd.n130 gnd.n129 1.10932
R716 gnd.n2 gnd.n1 1.1005
R717 gnd.n39 gnd.n38 1.1005
R718 gnd.n47 gnd.n46 1.1005
R719 gnd.n49 gnd.n48 1.1005
R720 gnd.n81 gnd.n52 0.846373
R721 gnd.n74 gnd.n52 0.816125
R722 gnd.n40 gnd.n17 0.552785
R723 gnd.n51 gnd.n37 0.550694
R724 gnd.n17 gnd.n16 0.539211
R725 gnd.n37 gnd.n36 0.520006
R726 gnd.n125 gnd.n107 0.470337
R727 gnd.n30 gnd.n20 0.445273
R728 gnd.n83 gnd.n4 0.444434
R729 gnd.n36 gnd.n22 0.438499
R730 gnd.n114 gnd.n83 0.420793
R731 gnd.n63 gnd.n20 0.419889
R732 gnd.n16 gnd.n3 0.418292
R733 gnd.n44 gnd.n21 0.408383
R734 gnd.n128 gnd.n127 0.407974
R735 gnd.n40 gnd.n18 0.395917
R736 gnd.n43 gnd.n42 0.37285
R737 gnd.n104 gnd.n18 0.347109
R738 gnd.n80 gnd.n63 0.343886
R739 gnd.n114 gnd.n84 0.343268
R740 gnd.n127 gnd.n4 0.318914
R741 gnd.n30 gnd.n21 0.318498
R742 gnd.n44 gnd.n22 0.306266
R743 gnd.n128 gnd.n3 0.305337
R744 gnd.n117 gnd.n84 0.294788
R745 gnd.n80 gnd.n79 0.294146
R746 gnd.n106 gnd.n105 0.288586
R747 gnd.n107 gnd.n106 0.288586
R748 gnd.n105 gnd.n104 0.249692
R749 gnd.n33 gnd.n32 0.247403
R750 gnd.n125 gnd.n124 0.244402
R751 gnd.n12 gnd.n10 0.24324
R752 gnd.n10 gnd.n4 0.227375
R753 gnd.n79 gnd.n78 0.227375
R754 gnd.n78 gnd.n63 0.227375
R755 gnd.n32 gnd.n30 0.227375
R756 gnd.n117 gnd.n116 0.227375
R757 gnd.n116 gnd.n114 0.227375
R758 gnd.n131 gnd.n130 0.17199
R759 gnd.n36 gnd.n23 0.0828779
R760 gnd.n16 gnd.n5 0.0744717
R761 gnd.n7 gnd.n6 0.0405896
R762 gnd.n13 gnd.n8 0.0405896
R763 gnd.n15 gnd.n6 0.0405896
R764 gnd.n8 gnd.n7 0.0405896
R765 gnd.n27 gnd.n25 0.0404028
R766 gnd.n29 gnd.n26 0.0404028
R767 gnd.n25 gnd.n24 0.0404028
R768 gnd.n27 gnd.n26 0.0404028
R769 gnd.n74 gnd.n53 0.0275956
R770 gnd.n124 gnd.n94 0.0275956
R771 gnd.n65 gnd.n54 0.0267868
R772 gnd.n109 gnd.n93 0.0267868
R773 gnd.n73 gnd.n55 0.0259779
R774 gnd.n122 gnd.n92 0.0259779
R775 gnd.n66 gnd.n56 0.0247647
R776 gnd.n110 gnd.n91 0.0247647
R777 gnd.n131 gnd.n0 0.02459
R778 gnd.n72 gnd.n57 0.0239559
R779 gnd.n121 gnd.n90 0.0239559
R780 gnd.n67 gnd.n58 0.0231471
R781 gnd.n111 gnd.n89 0.0231471
R782 gnd.n49 gnd.n46 0.023
R783 gnd.n39 gnd.n2 0.023
R784 gnd.n71 gnd.n59 0.0223382
R785 gnd.n120 gnd.n88 0.0223382
R786 gnd.n68 gnd.n60 0.021125
R787 gnd.n112 gnd.n87 0.021125
R788 gnd.n16 gnd.n15 0.0205448
R789 gnd.n13 gnd.n12 0.0205448
R790 gnd.n35 gnd.n24 0.0204514
R791 gnd.n33 gnd.n29 0.0204514
R792 gnd.n70 gnd.n61 0.0203162
R793 gnd.n119 gnd.n86 0.0203162
R794 gnd.n69 gnd.n62 0.0195074
R795 gnd.n113 gnd.n85 0.0195074
R796 gnd.n38 gnd.n1 0.01425
R797 gnd.n48 gnd.n47 0.01425
R798 gnd.n79 gnd.n76 0.0126324
R799 gnd.n118 gnd.n117 0.0126324
R800 gnd.n76 gnd.n62 0.0114191
R801 gnd.n118 gnd.n85 0.0114191
R802 gnd.n42 gnd.n38 0.01128
R803 gnd.n130 gnd.n1 0.01128
R804 gnd.n48 gnd.n43 0.01128
R805 gnd.n47 gnd.n0 0.01128
R806 gnd.n69 gnd.n61 0.0106103
R807 gnd.n113 gnd.n86 0.0106103
R808 gnd.n70 gnd.n60 0.00980147
R809 gnd.n119 gnd.n87 0.00980147
R810 gnd.n50 gnd.n49 0.00932
R811 gnd.n46 gnd.n45 0.00932
R812 gnd.n41 gnd.n39 0.00932
R813 gnd.n129 gnd.n2 0.00932
R814 gnd.n68 gnd.n59 0.00858823
R815 gnd.n112 gnd.n88 0.00858823
R816 gnd.n71 gnd.n58 0.00777941
R817 gnd.n120 gnd.n89 0.00777941
R818 gnd.n67 gnd.n57 0.00697059
R819 gnd.n111 gnd.n90 0.00697059
R820 gnd.n72 gnd.n56 0.00616176
R821 gnd.n121 gnd.n91 0.00616176
R822 gnd.n36 gnd.n35 0.00576316
R823 gnd.n66 gnd.n55 0.00494853
R824 gnd.n110 gnd.n92 0.00494853
R825 gnd.n73 gnd.n54 0.00413971
R826 gnd.n122 gnd.n93 0.00413971
R827 gnd.n65 gnd.n53 0.00333088
R828 gnd.n109 gnd.n94 0.00333088
R829 gnd.n131 gnd 0.0014625
R830 gnd.n126 gnd.n19 0.001
R831 gnd.n103 gnd.n102 0.001
R832 gnd.n99 gnd.n98 0.001
R833 gnd.n100 gnd.n97 0.001
R834 gnd.n96 gnd.n95 0.001
R835 gnd.n103 gnd.n19 0.001
R836 gnd.n126 gnd.n95 0.001
R837 gnd.n100 gnd.n96 0.001
R838 gnd.n99 gnd.n97 0.001
R839 gnd.n102 gnd.n98 0.001
C37 vbias gnd 2.83431f
C38 clk gnd 7.89606f
C39 out+ gnd 2.36194f
C40 out- gnd 2.35875f
C41 V+ gnd 3.9126f
C42 V- gnd 3.93119f
C43 vdd gnd 17.9739f
C44 a_1752_817# gnd 0.44266f $ **FLOATING
C45 a_944_1911# gnd 4.28617f $ **FLOATING
C46 a_687_2445# gnd 4.01269f $ **FLOATING
C47 a_1245_3300# gnd 1.43203f $ **FLOATING
.ends

.GLOBAL GND
.end
